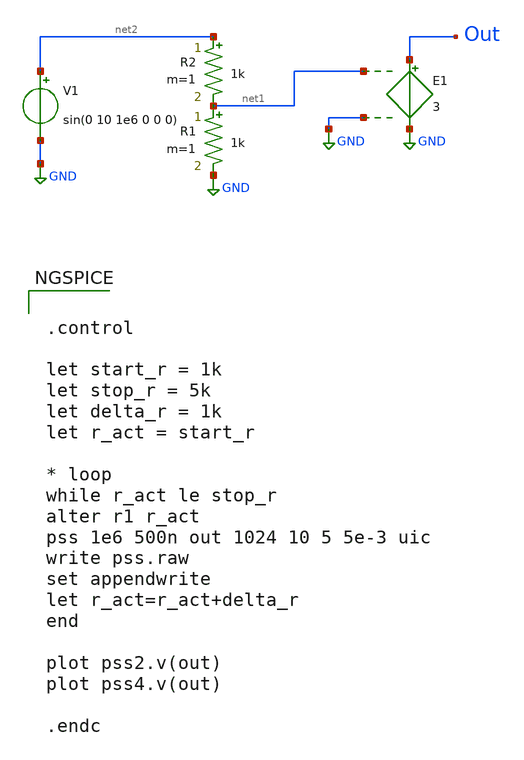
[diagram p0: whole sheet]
** sch_path: examples/xschem/pss.sch
**.subckt pss
E1 Out GND net1 GND 3
V1 net2 GND sin(0 10 1e6 0 0 0)
R2 net2 net1 1k m=1
R1 net1 GND 1k m=1
**** begin user architecture code


.control

let start_r = 1k
let stop_r = 5k
let delta_r = 1k
let r_act = start_r

* loop
while r_act le stop_r
alter r1 r_act
pss 1e6 500n out 1024 10 5 5e-3 uic
write pss.raw
set appendwrite
let r_act=r_act+delta_r
end

plot pss2.v(out)
plot pss4.v(out)

.endc


**** end user architecture code
**.ends
.GLOBAL GND
.end
